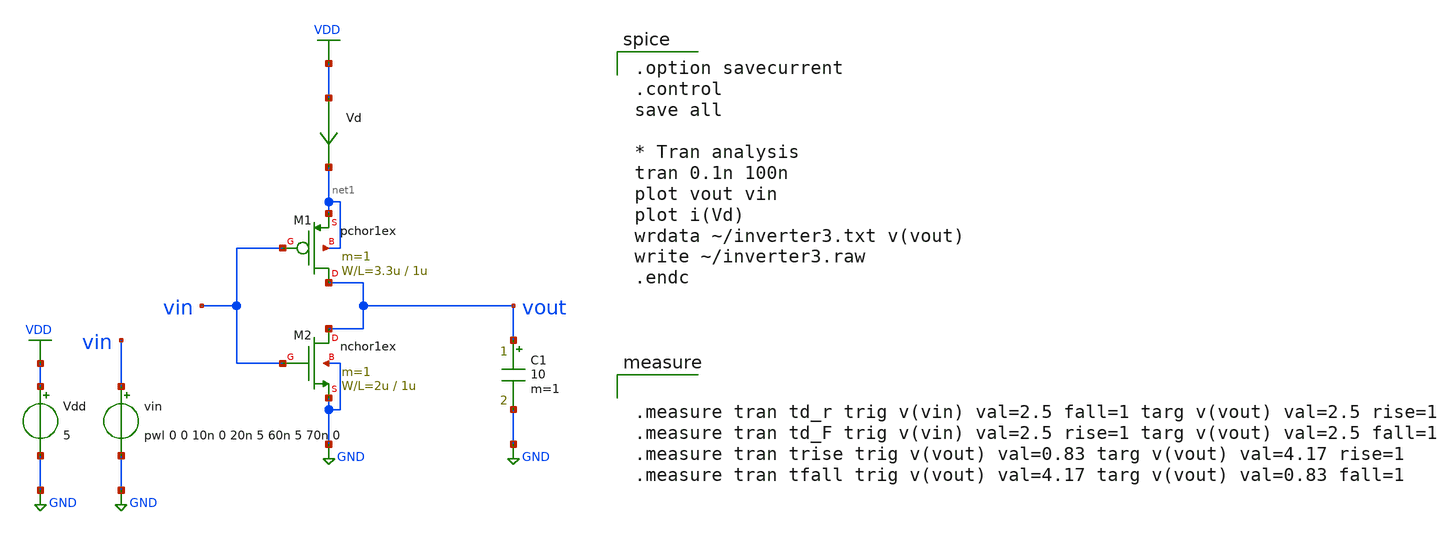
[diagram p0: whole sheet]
** sch_path: member_project/hiro-ogawa/others/inverter3.sch
**.subckt inverter3
Vdd VDD GND 5
vin vin GND pwl 0 0 10n 0 20n 5 60n 5 70n 0
Vd VDD net1 0
.save i(vd)
C1 vout GND 10 m=1
M1 vout vin net1 net1 pchor1ex L=1u W=3.3u m=1
M2 vout vin GND GND nchor1ex L=1u W=2u m=1
**** begin user architecture code
 .include $::LIB/mos.lib
.include $::LIB/passive.lib
.include $::LIB/diode.lib

.option savecurrent
.control
save all

* Tran analysis
tran 0.1n 100n
plot vout vin
plot i(Vd)
wrdata ~/inverter3.txt v(vout)
write ~/inverter3.raw
.endc




.measure tran td_r trig v(vin) val=2.5 fall=1 targ v(vout) val=2.5 rise=1
.measure tran td_F trig v(vin) val=2.5 rise=1 targ v(vout) val=2.5 fall=1
.measure tran trise trig v(vout) val=0.83 targ v(vout) val=4.17 rise=1
.measure tran tfall trig v(vout) val=4.17 targ v(vout) val=0.83 fall=1


**** end user architecture code
**.ends
.GLOBAL VDD
.GLOBAL GND
.end
